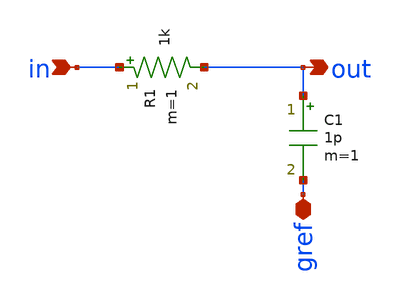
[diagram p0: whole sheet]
** sch_path: XSCHEM_DESIGNS/Filters/FirstOrder_RC_Filter.sch
**.subckt FirstOrder_RC_Filter in out gref
*.ipin in
*.opin out
*.iopin gref
R1 in out 1k m=1
C1 out gref 1p m=1
**.ends
.end
